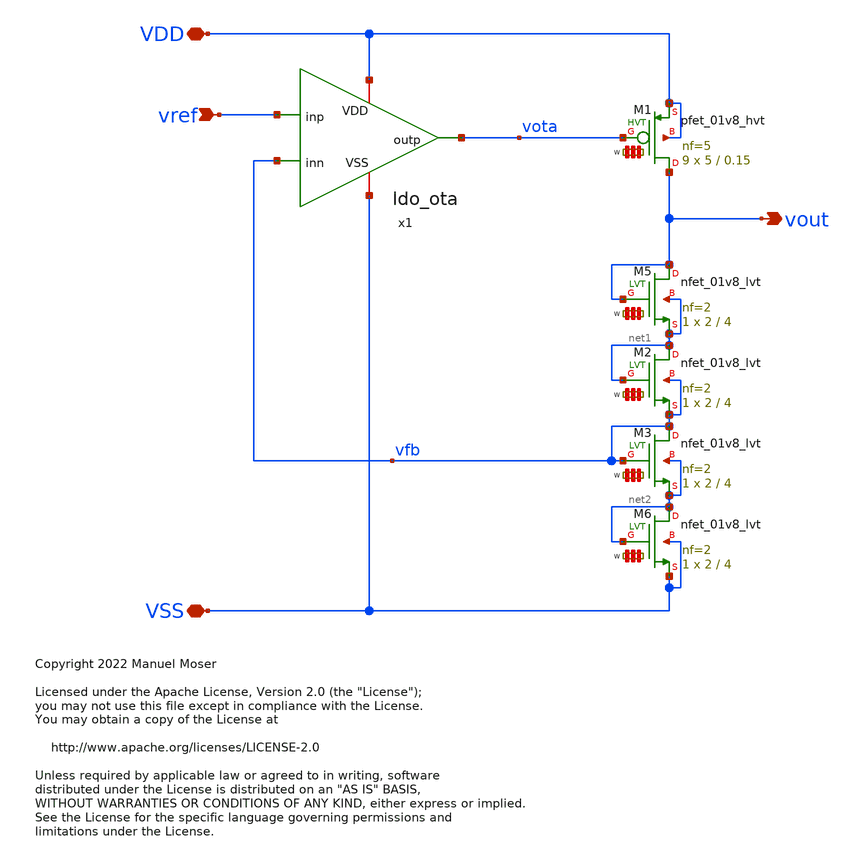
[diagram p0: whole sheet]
** sch_path: xschem/ldo.sch
* Copyright 2022 Manuel Moser
* Licensed under the Apache License, Version 2.0 (the "License");
**.subckt ldo vref VDD VSS vout
*.ipin vref
*.iopin VDD
*.iopin VSS
*.opin vout
x1 VDD vref vota vfb VSS ldo_ota
XM1 vout vota VDD VDD sky130_fd_pr__pfet_01v8_hvt L=0.15 W='5 * 5 ' nf=5 ad='int((nf+1)/2) * W / nf * 0.29'
+ as='int((nf+2)/2) * W / nf * 0.29' pd='2*int((nf+1)/2) * (W / nf + 0.29)' ps='2*int((nf+2)/2) * (W / nf + 0.29)'
+ nrd='0.29 / W ' nrs='0.29 / W ' sa=0 sb=0 sd=0 mult=9 m=9
XM5 vout vout net1 net1 sky130_fd_pr__nfet_01v8_lvt L=4 W='2 * 2 ' nf=2 ad='int((nf+1)/2) * W/nf * 0.29'
+ as='int((nf+2)/2) * W/nf * 0.29' pd='2*int((nf+1)/2) * (W/nf + 0.29)' ps='2*int((nf+2)/2) * (W/nf + 0.29)'
+ nrd='0.29 / W' nrs='0.29 / W' sa=0 sb=0 sd=0 mult=1 m=1
XM2 net1 net1 vfb vfb sky130_fd_pr__nfet_01v8_lvt L=4 W='2 * 2 ' nf=2 ad='int((nf+1)/2) * W/nf * 0.29'
+ as='int((nf+2)/2) * W/nf * 0.29' pd='2*int((nf+1)/2) * (W/nf + 0.29)' ps='2*int((nf+2)/2) * (W/nf + 0.29)'
+ nrd='0.29 / W' nrs='0.29 / W' sa=0 sb=0 sd=0 mult=1 m=1
XM3 vfb vfb net2 net2 sky130_fd_pr__nfet_01v8_lvt L=4 W='2 * 2 ' nf=2 ad='int((nf+1)/2) * W/nf * 0.29'
+ as='int((nf+2)/2) * W/nf * 0.29' pd='2*int((nf+1)/2) * (W/nf + 0.29)' ps='2*int((nf+2)/2) * (W/nf + 0.29)'
+ nrd='0.29 / W' nrs='0.29 / W' sa=0 sb=0 sd=0 mult=1 m=1
XM6 net2 net2 VSS VSS sky130_fd_pr__nfet_01v8_lvt L=4 W='2 * 2 ' nf=2 ad='int((nf+1)/2) * W/nf * 0.29'
+ as='int((nf+2)/2) * W/nf * 0.29' pd='2*int((nf+1)/2) * (W/nf + 0.29)' ps='2*int((nf+2)/2) * (W/nf + 0.29)'
+ nrd='0.29 / W' nrs='0.29 / W' sa=0 sb=0 sd=0 mult=1 m=1
**.ends
.end
